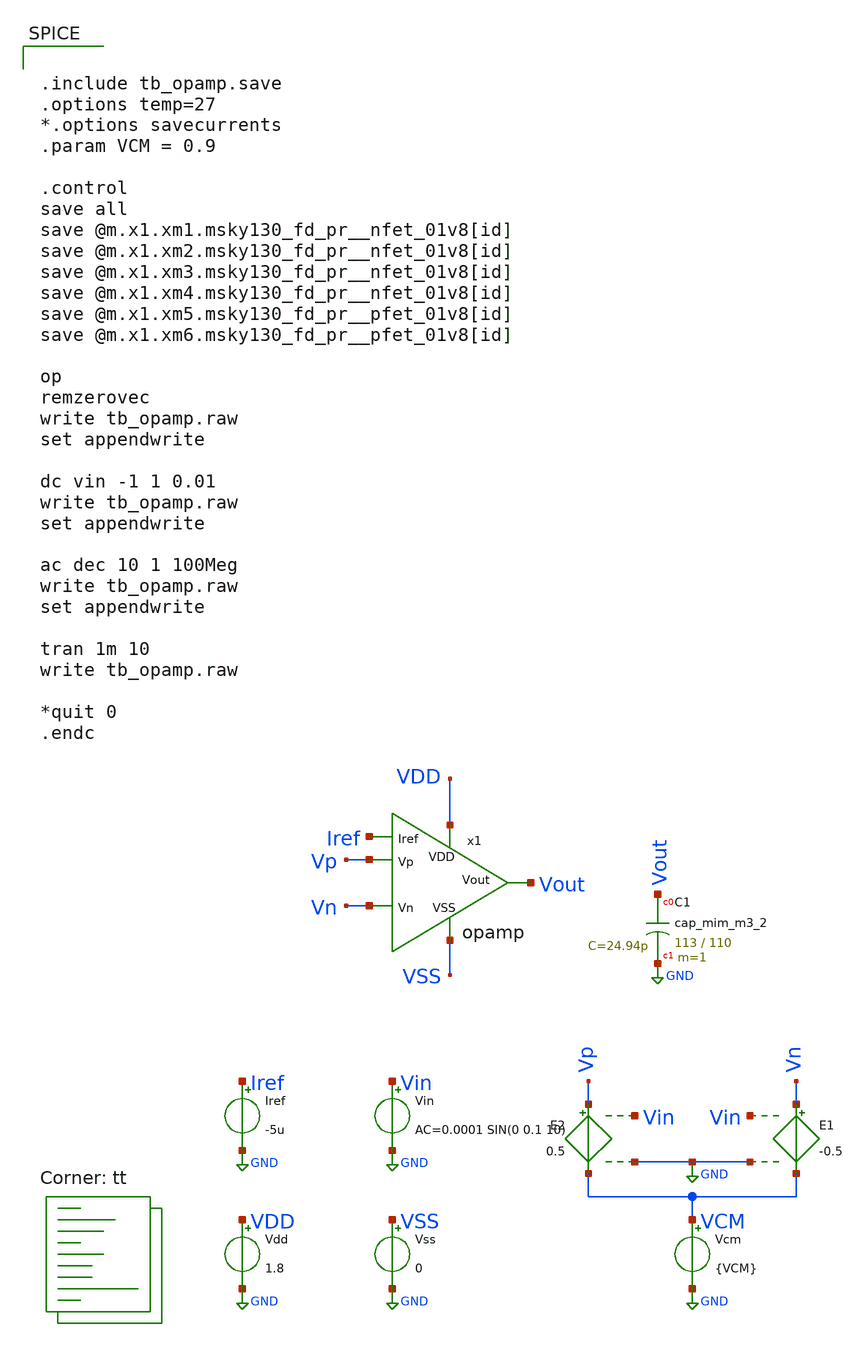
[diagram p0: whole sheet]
** sch_path: xschem/tb_opamp.sch
**.subckt tb_opamp
Vdd VDD GND 1.8
Vss VSS GND 0
E1 Vn VCM Vin GND -0.5
Vcm VCM GND {VCM}
E2 Vp VCM Vin GND 0.5
Vin Vin GND AC=0.0001 SIN(0 0.1 10)
Iref Iref GND -5u
XC1 Vout GND sky130_fd_pr__cap_mim_m3_2 W=113 L=110 MF=1 m=1
x1 Vout Vn Vp VSS Iref VDD opamp
**** begin user architecture code


.include tb_opamp.save
.options temp=27
*.options savecurrents
.param VCM = 0.9

.control
save all
save @m.x1.xm1.msky130_fd_pr__nfet_01v8[id]
save @m.x1.xm2.msky130_fd_pr__nfet_01v8[id]
save @m.x1.xm3.msky130_fd_pr__nfet_01v8[id]
save @m.x1.xm4.msky130_fd_pr__nfet_01v8[id]
save @m.x1.xm5.msky130_fd_pr__pfet_01v8[id]
save @m.x1.xm6.msky130_fd_pr__pfet_01v8[id]

op
remzerovec
write tb_opamp.raw
set appendwrite

dc vin -1 1 0.01
write tb_opamp.raw
set appendwrite

ac dec 10 1 100Meg
write tb_opamp.raw
set appendwrite

tran 1m 10
write tb_opamp.raw

*quit 0
.endc


.lib $::SKYWATER_MODELS/sky130.lib.spice tt
**** end user architecture code
**.ends

* expanding   symbol:  /foss/designs/ttsky_opamp/xschem/opamp.sym # of pins=6
** sym_path: xschem/opamp.sym
** sch_path: xschem/opamp.sch
.subckt opamp Vout Vn Vp VSS Iref VDD
*.ipin VSS
*.ipin Vp
*.opin Vout
*.ipin Vn
*.ipin VDD
*.ipin Iref
XM1 Iref Iref VSS VSS sky130_fd_pr__nfet_01v8 L=1 W=10 nf=8 ad='int((8 + 1)/2) * 10 / 8 * 0.29' as='int((8 + 2)/2) * 10 / 8 * 0.29'
+ pd='2*int((8 + 1)/2) * (10 / 8 + 0.29)' ps='2*int((8 + 2)/2) * (10 / 8 + 0.29)' nrd='0.29 / 10 ' nrs='0.29 / 10 '
+ sa=0 sb=0 sd=0 mult=1 m=1
XM2 Vx Iref VSS VSS sky130_fd_pr__nfet_01v8 L=1 W=10 nf=8 ad='int((8 + 1)/2) * 10 / 8 * 0.29' as='int((8 + 2)/2) * 10 / 8 * 0.29'
+ pd='2*int((8 + 1)/2) * (10 / 8 + 0.29)' ps='2*int((8 + 2)/2) * (10 / 8 + 0.29)' nrd='0.29 / 10 ' nrs='0.29 / 10 '
+ sa=0 sb=0 sd=0 mult=1 m=1
XM3 Vout Vp Vx VSS sky130_fd_pr__nfet_01v8 L=4 W=400 nf=1 ad='int((1 + 1)/2) * 400 / 1 * 0.29' as='int((1 + 2)/2) * 400 / 1 * 0.29'
+ pd='2*int((1 + 1)/2) * (400 / 1 + 0.29)' ps='2*int((1 + 2)/2) * (400 / 1 + 0.29)' nrd='0.29 / 400 ' nrs='0.29 / 400 '
+ sa=0 sb=0 sd=0 mult=1 m=1
XM4 Vg1 Vn Vx VSS sky130_fd_pr__nfet_01v8 L=4 W=400 nf=1 ad='int((1 + 1)/2) * 400 / 1 * 0.29' as='int((1 + 2)/2) * 400 / 1 * 0.29'
+ pd='2*int((1 + 1)/2) * (400 / 1 + 0.29)' ps='2*int((1 + 2)/2) * (400 / 1 + 0.29)' nrd='0.29 / 400 ' nrs='0.29 / 400 '
+ sa=0 sb=0 sd=0 mult=1 m=1
XM5 Vout Vg1 VDD VDD sky130_fd_pr__pfet_01v8 L=4 W=4 nf=2 ad='int((2 + 1)/2) * 4 / 2 * 0.29' as='int((2 + 2)/2) * 4 / 2 * 0.29'
+ pd='2*int((2 + 1)/2) * (4 / 2 + 0.29)' ps='2*int((2 + 2)/2) * (4 / 2 + 0.29)' nrd='0.29 / 4 ' nrs='0.29 / 4 '
+ sa=0 sb=0 sd=0 mult=1 m=1
XM6 Vg1 Vg1 VDD VDD sky130_fd_pr__pfet_01v8 L=4 W=4 nf=2 ad='int((2 + 1)/2) * 4 / 2 * 0.29' as='int((2 + 2)/2) * 4 / 2 * 0.29'
+ pd='2*int((2 + 1)/2) * (4 / 2 + 0.29)' ps='2*int((2 + 2)/2) * (4 / 2 + 0.29)' nrd='0.29 / 4 ' nrs='0.29 / 4 '
+ sa=0 sb=0 sd=0 mult=1 m=1
XM7 net1 Iref VSS VSS sky130_fd_pr__nfet_01v8 L=1 W=10 nf=8 ad='int((8 + 1)/2) * 10 / 8 * 0.29' as='int((8 + 2)/2) * 10 / 8 * 0.29'
+ pd='2*int((8 + 1)/2) * (10 / 8 + 0.29)' ps='2*int((8 + 2)/2) * (10 / 8 + 0.29)' nrd='0.29 / 10 ' nrs='0.29 / 10 '
+ sa=0 sb=0 sd=0 mult=1 m=1
XM8 net2 VDD VDD VDD sky130_fd_pr__pfet_01v8 L=4 W=4 nf=2 ad='int((2 + 1)/2) * 4 / 2 * 0.29' as='int((2 + 2)/2) * 4 / 2 * 0.29'
+ pd='2*int((2 + 1)/2) * (4 / 2 + 0.29)' ps='2*int((2 + 2)/2) * (4 / 2 + 0.29)' nrd='0.29 / 4 ' nrs='0.29 / 4 '
+ sa=0 sb=0 sd=0 mult=1 m=1
.ends

.GLOBAL GND
.GLOBAL VDD
.end
